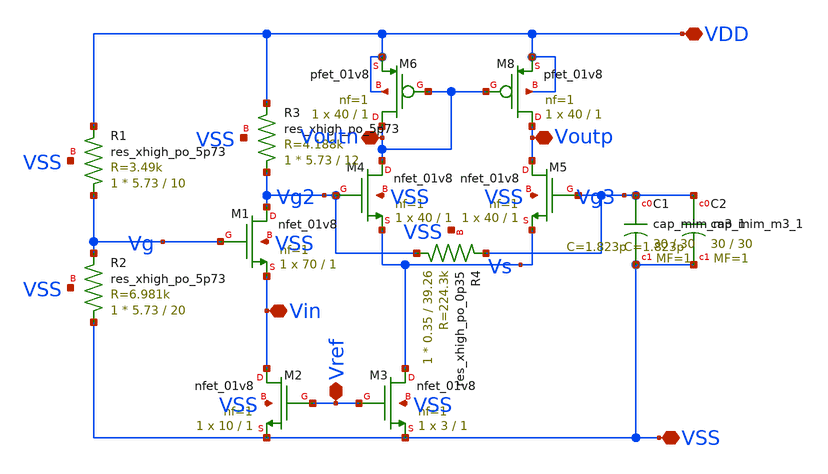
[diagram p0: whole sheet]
** sch_path: Project/xschem/lna.sch
**.subckt lna VSS VDD Voutp Voutn Vref Vin
*.iopin VSS
*.iopin VDD
*.iopin Voutp
*.iopin Voutn
*.iopin Vref
*.iopin Vin
XR1 Vg VDD VSS sky130_fd_pr__res_xhigh_po_5p73 L=10 mult=1 m=1
XR2 VSS Vg VSS sky130_fd_pr__res_xhigh_po_5p73 L=20 mult=1 m=1
XM1 Vg2 Vg Vin VSS sky130_fd_pr__nfet_01v8 L=1 W=70 nf=1 ad='int((nf+1)/2) * W/nf * 0.29' as='int((nf+2)/2) * W/nf * 0.29'
+ pd='2*int((nf+1)/2) * (W/nf + 0.29)' ps='2*int((nf+2)/2) * (W/nf + 0.29)' nrd='0.29 / W' nrs='0.29 / W'
+ sa=0 sb=0 sd=0 mult=1 m=1
XM2 Vin Vref VSS VSS sky130_fd_pr__nfet_01v8 L=1 W=10 nf=1 ad='int((nf+1)/2) * W/nf * 0.29' as='int((nf+2)/2) * W/nf * 0.29'
+ pd='2*int((nf+1)/2) * (W/nf + 0.29)' ps='2*int((nf+2)/2) * (W/nf + 0.29)' nrd='0.29 / W' nrs='0.29 / W'
+ sa=0 sb=0 sd=0 mult=1 m=1
XM3 Vs Vref VSS VSS sky130_fd_pr__nfet_01v8 L=1 W=3 nf=1 ad='int((nf+1)/2) * W/nf * 0.29' as='int((nf+2)/2) * W/nf * 0.29'
+ pd='2*int((nf+1)/2) * (W/nf + 0.29)' ps='2*int((nf+2)/2) * (W/nf + 0.29)' nrd='0.29 / W' nrs='0.29 / W'
+ sa=0 sb=0 sd=0 mult=1 m=1
XM4 Voutn Vg2 Vs VSS sky130_fd_pr__nfet_01v8 L=1 W=40 nf=1 ad='int((nf+1)/2) * W/nf * 0.29' as='int((nf+2)/2) * W/nf * 0.29'
+ pd='2*int((nf+1)/2) * (W/nf + 0.29)' ps='2*int((nf+2)/2) * (W/nf + 0.29)' nrd='0.29 / W' nrs='0.29 / W'
+ sa=0 sb=0 sd=0 mult=1 m=1
XM5 Voutp Vg3 Vs VSS sky130_fd_pr__nfet_01v8 L=1 W=40 nf=1 ad='int((nf+1)/2) * W/nf * 0.29' as='int((nf+2)/2) * W/nf * 0.29'
+ pd='2*int((nf+1)/2) * (W/nf + 0.29)' ps='2*int((nf+2)/2) * (W/nf + 0.29)' nrd='0.29 / W' nrs='0.29 / W'
+ sa=0 sb=0 sd=0 mult=1 m=1
XR3 Vg2 VDD VSS sky130_fd_pr__res_xhigh_po_5p73 L=12 mult=1 m=1
XM8 Voutp Voutn VDD VDD sky130_fd_pr__pfet_01v8 L=1 W=40 nf=1 ad='int((nf+1)/2) * W/nf * 0.29' as='int((nf+2)/2) * W/nf * 0.29'
+ pd='2*int((nf+1)/2) * (W/nf + 0.29)' ps='2*int((nf+2)/2) * (W/nf + 0.29)' nrd='0.29 / W' nrs='0.29 / W'
+ sa=0 sb=0 sd=0 mult=1 m=1
XM6 Voutn Voutn VDD VDD sky130_fd_pr__pfet_01v8 L=1 W=40 nf=1 ad='int((nf+1)/2) * W/nf * 0.29' as='int((nf+2)/2) * W/nf * 0.29'
+ pd='2*int((nf+1)/2) * (W/nf + 0.29)' ps='2*int((nf+2)/2) * (W/nf + 0.29)' nrd='0.29 / W' nrs='0.29 / W'
+ sa=0 sb=0 sd=0 mult=1 m=1
XC1 Vg3 VSS sky130_fd_pr__cap_mim_m3_1 W=30 L=30 MF=1 m=1
XC2 Vg3 VSS sky130_fd_pr__cap_mim_m3_1 W=30 L=30 MF=1 m=1
XR4 Vg2 Vg3 VSS sky130_fd_pr__res_xhigh_po_0p35 L=39.26 mult=1 m=1
**.ends
.end
